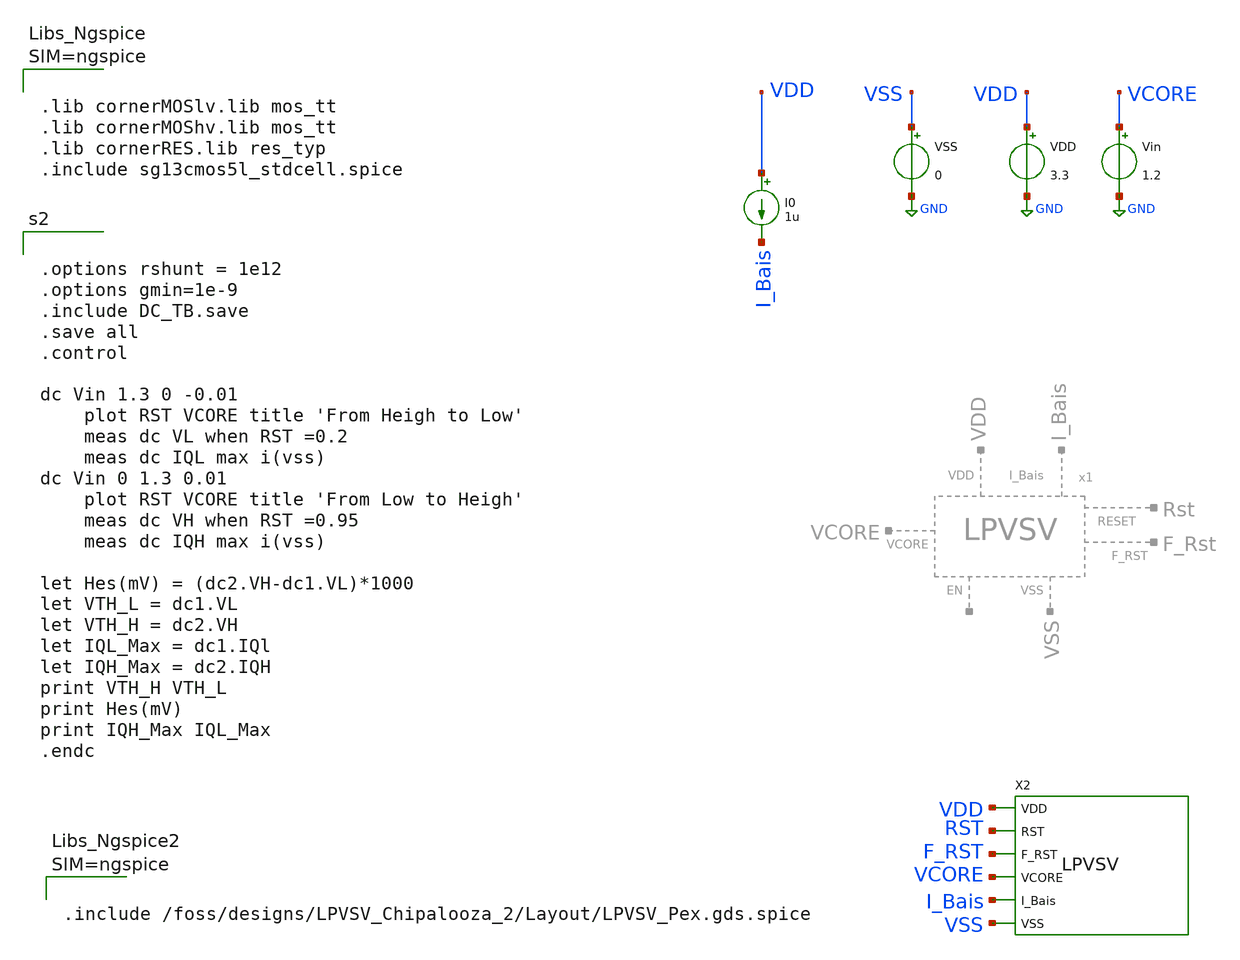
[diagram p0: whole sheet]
** sch_path: Simulation/DC_TB.sch
**.subckt DC_TB
VDD VDD GND 3.3
VSS VSS GND 0
Vin VCORE GND 1.2
I0 VDD I_Bais 1u
X2 VSS F_RST VDD VCORE I_Bais RST LPVSV
**** begin user architecture code


.options rshunt = 1e12
.options gmin=1e-9
.include DC_TB.save
.save all
.control

dc Vin 1.3 0 -0.01
	plot RST VCORE title 'From Heigh to Low'
	meas dc VL when RST =0.2
	meas dc IQL max i(vss)
dc Vin 0 1.3 0.01
	plot RST VCORE title 'From Low to Heigh'
	meas dc VH when RST =0.95
	meas dc IQH max i(vss)

let Hes(mV) = (dc2.VH-dc1.VL)*1000
let VTH_L = dc1.VL
let VTH_H = dc2.VH
let IQL_Max = dc1.IQl
let IQH_Max = dc2.IQH
print VTH_H VTH_L
print Hes(mV)
print IQH_Max IQL_Max
.endc




.options rshunt = 1e15
.options gmin=1e-9
.options reltol = 0.01 abstol = 1p
.option filetype=ascii





.lib cornerMOSlv.lib mos_tt
.lib cornerMOShv.lib mos_tt
.lib cornerRES.lib res_typ
.include sg13cmos5l_stdcell.spice






.include /foss/designs/LPVSV_Chipalooza_2/Layout/LPVSV_Pex.gds.spice



**** end user architecture code
**.ends
.GLOBAL GND
.end
